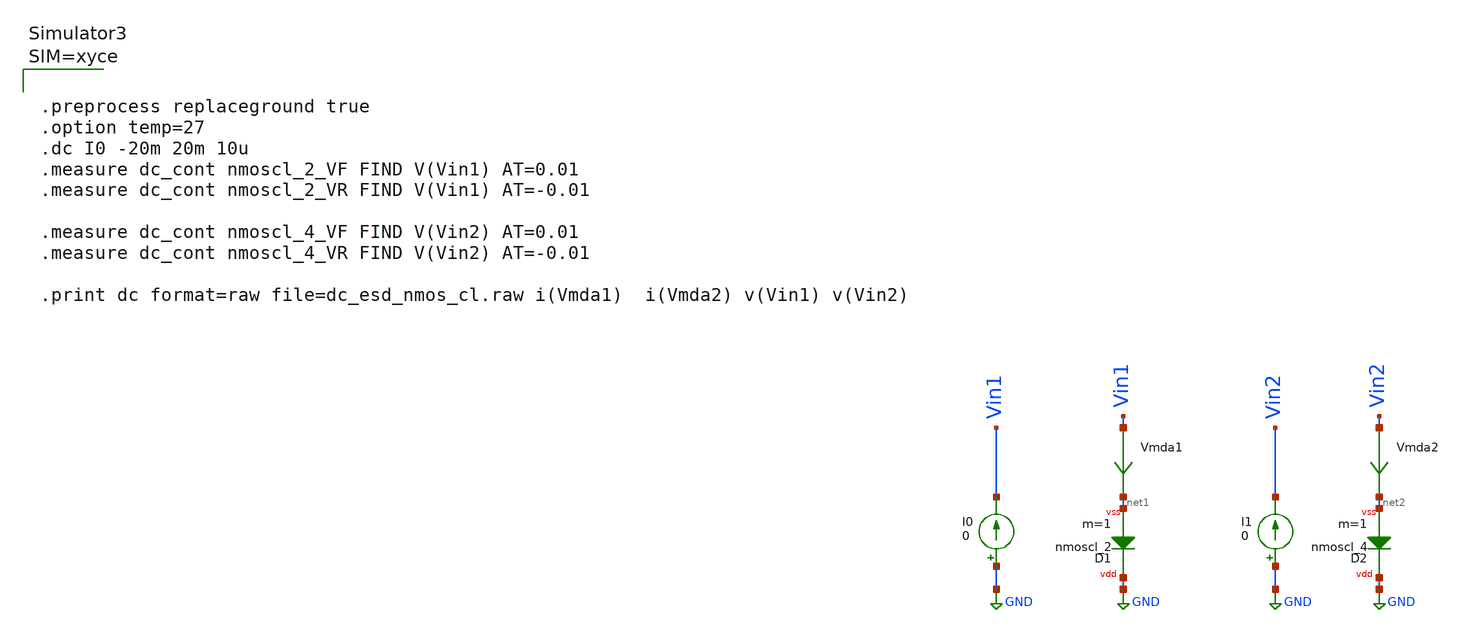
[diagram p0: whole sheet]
** sch_path: ihp-sg13g2/libs.tech/xschem/sg13g2_tests_xyce/dc_esd_nmos_cl.sch
**.subckt dc_esd_nmos_cl
Vmda1 Vin1 net1 0
.save i(vmda1)
I0 GND Vin1 0
Vmda2 Vin2 net2 0
.save i(vmda2)
I1 GND Vin2 0
XD1 net1 GND nmoscl_2 m=1
XD2 net2 GND nmoscl_4 m=1
**** begin user architecture code






.lib cornerMOSlv.lib mos_tt





.param temp=27
.control
save all
dc I0 -20m 20m 10u
*dc I1 -20m 20m 10u

echo ---------nmoscl_2---------
meas dc Vf FIND v(Vin1) AT=0.01
meas dc Vr FIND v(Vin1) AT=-0.01

echo ---------nmoscl_4---------
*meas dc Vf FIND v(Vin2) AT=0.01
*meas dc Vr FIND v(Vin2) AT=-0.01

write dc_esd_nmos_cl.raw
.endc






**** end user architecture code
**.ends
.GLOBAL GND
.end
